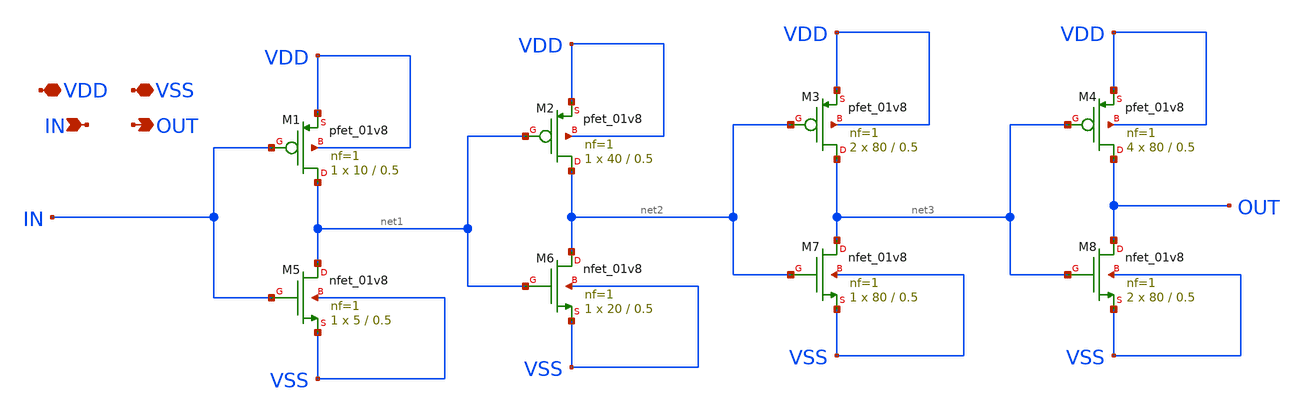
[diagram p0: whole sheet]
** sch_path: Xschem/TOP/Tappered-Buffer_1.sch
**.subckt Tappered-Buffer_1 VDD VSS IN OUT
*.iopin VDD
*.iopin VSS
*.ipin IN
*.opin OUT
XM1 net1 IN VDD VDD sky130_fd_pr__pfet_01v8 L=0.5 W=10 nf=1 ad='int((nf+1)/2) * W/nf * 0.29' as='int((nf+2)/2) * W/nf * 0.29'
+ pd='2*int((nf+1)/2) * (W/nf + 0.29)' ps='2*int((nf+2)/2) * (W/nf + 0.29)' nrd='0.29 / W' nrs='0.29 / W'
+ sa=0 sb=0 sd=0 mult=1 m=1
XM2 net2 net1 VDD VDD sky130_fd_pr__pfet_01v8 L=0.5 W=40 nf=1 ad='int((nf+1)/2) * W/nf * 0.29' as='int((nf+2)/2) * W/nf * 0.29'
+ pd='2*int((nf+1)/2) * (W/nf + 0.29)' ps='2*int((nf+2)/2) * (W/nf + 0.29)' nrd='0.29 / W' nrs='0.29 / W'
+ sa=0 sb=0 sd=0 mult=1 m=1
XM3 net3 net2 VDD VDD sky130_fd_pr__pfet_01v8 L=0.5 W=80 nf=1 ad='int((nf+1)/2) * W/nf * 0.29' as='int((nf+2)/2) * W/nf * 0.29'
+ pd='2*int((nf+1)/2) * (W/nf + 0.29)' ps='2*int((nf+2)/2) * (W/nf + 0.29)' nrd='0.29 / W' nrs='0.29 / W'
+ sa=0 sb=0 sd=0 mult=2 m=2
XM5 net1 IN VSS VSS sky130_fd_pr__nfet_01v8 L=0.5 W=5 nf=1 ad='int((nf+1)/2) * W/nf * 0.29' as='int((nf+2)/2) * W/nf * 0.29'
+ pd='2*int((nf+1)/2) * (W/nf + 0.29)' ps='2*int((nf+2)/2) * (W/nf + 0.29)' nrd='0.29 / W' nrs='0.29 / W'
+ sa=0 sb=0 sd=0 mult=1 m=1
XM6 net2 net1 VSS VSS sky130_fd_pr__nfet_01v8 L=0.5 W=20 nf=1 ad='int((nf+1)/2) * W/nf * 0.29' as='int((nf+2)/2) * W/nf * 0.29'
+ pd='2*int((nf+1)/2) * (W/nf + 0.29)' ps='2*int((nf+2)/2) * (W/nf + 0.29)' nrd='0.29 / W' nrs='0.29 / W'
+ sa=0 sb=0 sd=0 mult=1 m=1
XM7 net3 net2 VSS VSS sky130_fd_pr__nfet_01v8 L=0.5 W=80 nf=1 ad='int((nf+1)/2) * W/nf * 0.29' as='int((nf+2)/2) * W/nf * 0.29'
+ pd='2*int((nf+1)/2) * (W/nf + 0.29)' ps='2*int((nf+2)/2) * (W/nf + 0.29)' nrd='0.29 / W' nrs='0.29 / W'
+ sa=0 sb=0 sd=0 mult=1 m=1
XM4 OUT net3 VDD VDD sky130_fd_pr__pfet_01v8 L=0.5 W=80 nf=1 ad='int((nf+1)/2) * W/nf * 0.29' as='int((nf+2)/2) * W/nf * 0.29'
+ pd='2*int((nf+1)/2) * (W/nf + 0.29)' ps='2*int((nf+2)/2) * (W/nf + 0.29)' nrd='0.29 / W' nrs='0.29 / W'
+ sa=0 sb=0 sd=0 mult=4 m=4
XM8 OUT net3 VSS VSS sky130_fd_pr__nfet_01v8 L=0.5 W=80 nf=1 ad='int((nf+1)/2) * W/nf * 0.29' as='int((nf+2)/2) * W/nf * 0.29'
+ pd='2*int((nf+1)/2) * (W/nf + 0.29)' ps='2*int((nf+2)/2) * (W/nf + 0.29)' nrd='0.29 / W' nrs='0.29 / W'
+ sa=0 sb=0 sd=0 mult=2 m=2
**.ends
.end
